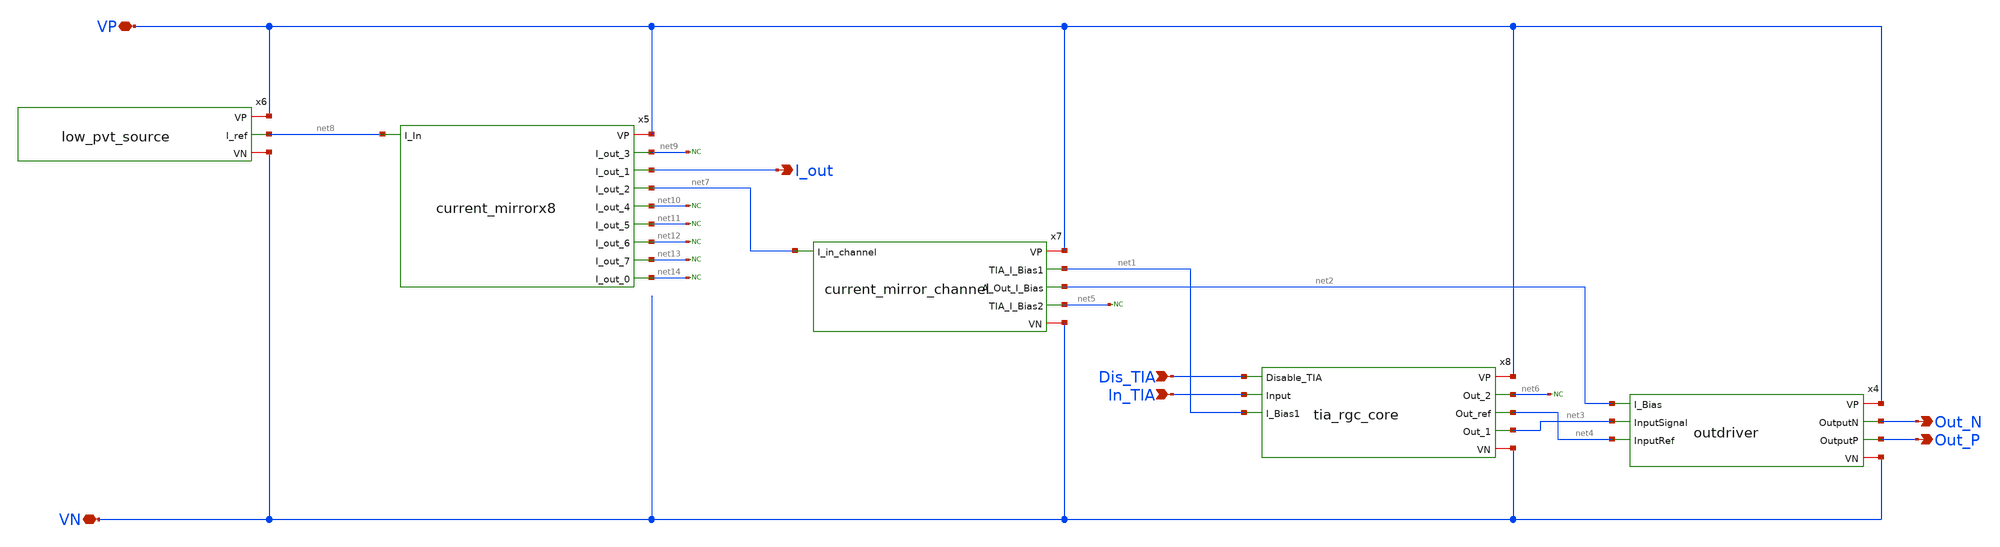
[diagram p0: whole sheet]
** sch_path: xschem/mpw5_submission.sch
**.subckt mpw5_submission VP In_TIA Out_N VN Out_P Dis_TIA I_out
*.iopin VP
*.ipin In_TIA
*.opin Out_N
*.iopin VN
*.opin Out_P
*.ipin Dis_TIA
*.opin I_out
x4 VP Out_N Out_P net2 net3 net4 VN outdriver
x5 VP net9 I_out net7 net8 net10 net11 net12 net13 net14 current_mirrorx8
x6 VP net8 VN low_pvt_source
x7 VP net1 net2 net5 net7 VN current_mirror_channel
x8 VP net6 net4 net3 Dis_TIA In_TIA net1 VN tia_rgc_core
* noconn #net5
* noconn #net6
* noconn #net9
* noconn #net10
* noconn #net11
* noconn #net12
* noconn #net13
* noconn #net14
**.ends

* expanding   symbol:  outdriver/outdriver.sym # of pins=7
** sym_path: xschem/outdriver/outdriver.sym
** sch_path: xschem/outdriver/outdriver.sch
.subckt outdriver VP OutputN OutputP I_Bias InputSignal InputRef VN
*.iopin VN
*.ipin InputRef
*.iopin VP
*.ipin I_Bias
*.ipin InputSignal
*.opin OutputN
*.opin OutputP
XM1 V_da1_P InputSignal VM6D VM6D sky130_fd_pr__nfet_01v8_lvt L=0.15 W=2 nf=1 ad='int((nf+1)/2) * W/nf * 0.29'
+ as='int((nf+2)/2) * W/nf * 0.29' pd='2*int((nf+1)/2) * (W/nf + 0.29)' ps='2*int((nf+2)/2) * (W/nf + 0.29)'
+ nrd='0.29 / W' nrs='0.29 / W' sa=0 sb=0 sd=0 mult=11*2 m=11*2
XM3 VM3D I_Bias VN VN sky130_fd_pr__nfet_01v8 L=0.5 W=2 nf=1 ad='int((nf+1)/2) * W/nf * 0.29' as='int((nf+2)/2) * W/nf * 0.29'
+ pd='2*int((nf+1)/2) * (W/nf + 0.29)' ps='2*int((nf+2)/2) * (W/nf + 0.29)' nrd='0.29 / W' nrs='0.29 / W'
+ sa=0 sb=0 sd=0 mult=2*(64) m=2*(64)
XM6 VM6D I_Bias VM3D VN sky130_fd_pr__nfet_01v8 L=0.15 W=2 nf=1 ad='int((nf+1)/2) * W/nf * 0.29' as='int((nf+2)/2) * W/nf * 0.29'
+ pd='2*int((nf+1)/2) * (W/nf + 0.29)' ps='2*int((nf+2)/2) * (W/nf + 0.29)' nrd='0.29 / W' nrs='0.29 / W'
+ sa=0 sb=0 sd=0 mult=64 m=64
XM7 I_Bias I_Bias net1 VN sky130_fd_pr__nfet_01v8 L=0.15 W=2 nf=1 ad='int((nf+1)/2) * W/nf * 0.29' as='int((nf+2)/2) * W/nf * 0.29'
+ pd='2*int((nf+1)/2) * (W/nf + 0.29)' ps='2*int((nf+2)/2) * (W/nf + 0.29)' nrd='0.29 / W' nrs='0.29 / W'
+ sa=0 sb=0 sd=0 mult=2 m=2
XM8 net1 I_Bias VN VN sky130_fd_pr__nfet_01v8 L=0.5 W=2 nf=1 ad='int((nf+1)/2) * W/nf * 0.29' as='int((nf+2)/2) * W/nf * 0.29'
+ pd='2*int((nf+1)/2) * (W/nf + 0.29)' ps='2*int((nf+2)/2) * (W/nf + 0.29)' nrd='0.29 / W' nrs='0.29 / W'
+ sa=0 sb=0 sd=0 mult=2*2 m=2*2
XM2 V_da2_P V_da1_P VM1_D VM1_D sky130_fd_pr__nfet_01v8_lvt L=0.15 W=2 nf=1 ad='int((nf+1)/2) * W/nf * 0.29'
+ as='int((nf+2)/2) * W/nf * 0.29' pd='2*int((nf+1)/2) * (W/nf + 0.29)' ps='2*int((nf+2)/2) * (W/nf + 0.29)'
+ nrd='0.29 / W' nrs='0.29 / W' sa=0 sb=0 sd=0 mult=44*2 m=44*2
XM4 V_da2_N V_da1_N VM1_D VM1_D sky130_fd_pr__nfet_01v8_lvt L=0.15 W=2 nf=1 ad='int((nf+1)/2) * W/nf * 0.29'
+ as='int((nf+2)/2) * W/nf * 0.29' pd='2*int((nf+1)/2) * (W/nf + 0.29)' ps='2*int((nf+2)/2) * (W/nf + 0.29)'
+ nrd='0.29 / W' nrs='0.29 / W' sa=0 sb=0 sd=0 mult=44*2 m=44*2
XM9 net2 I_Bias VN VN sky130_fd_pr__nfet_01v8 L=0.5 W=2 nf=1 ad='int((nf+1)/2) * W/nf * 0.29' as='int((nf+2)/2) * W/nf * 0.29'
+ pd='2*int((nf+1)/2) * (W/nf + 0.29)' ps='2*int((nf+2)/2) * (W/nf + 0.29)' nrd='0.29 / W' nrs='0.29 / W'
+ sa=0 sb=0 sd=0 mult=2*(256+64) m=2*(256+64)
XM10 VM1_D I_Bias net2 VN sky130_fd_pr__nfet_01v8 L=0.15 W=2 nf=1 ad='int((nf+1)/2) * W/nf * 0.29' as='int((nf+2)/2) * W/nf * 0.29'
+ pd='2*int((nf+1)/2) * (W/nf + 0.29)' ps='2*int((nf+2)/2) * (W/nf + 0.29)' nrd='0.29 / W' nrs='0.29 / W'
+ sa=0 sb=0 sd=0 mult=256+64 m=256+64
XM11 OutputP V_da2_P VM14D VM14D sky130_fd_pr__nfet_01v8_lvt L=0.15 W=2 nf=1 ad='int((nf+1)/2) * W/nf * 0.29'
+ as='int((nf+2)/2) * W/nf * 0.29' pd='2*int((nf+1)/2) * (W/nf + 0.29)' ps='2*int((nf+2)/2) * (W/nf + 0.29)'
+ nrd='0.29 / W' nrs='0.29 / W' sa=0 sb=0 sd=0 mult=44*4*2 m=44*4*2
XM12 OutputN V_da2_N VM14D VM14D sky130_fd_pr__nfet_01v8_lvt L=0.15 W=2 nf=1 ad='int((nf+1)/2) * W/nf * 0.29'
+ as='int((nf+2)/2) * W/nf * 0.29' pd='2*int((nf+1)/2) * (W/nf + 0.29)' ps='2*int((nf+2)/2) * (W/nf + 0.29)'
+ nrd='0.29 / W' nrs='0.29 / W' sa=0 sb=0 sd=0 mult=44*4*2 m=44*4*2
XM13 net3 I_Bias VN VN sky130_fd_pr__nfet_01v8 L=0.5 W=2 nf=1 ad='int((nf+1)/2) * W/nf * 0.29' as='int((nf+2)/2) * W/nf * 0.29'
+ pd='2*int((nf+1)/2) * (W/nf + 0.29)' ps='2*int((nf+2)/2) * (W/nf + 0.29)' nrd='0.29 / W' nrs='0.29 / W'
+ sa=0 sb=0 sd=0 mult=2*(1024+256) m=2*(1024+256)
XM14 VM14D I_Bias net3 VN sky130_fd_pr__nfet_01v8 L=0.15 W=2 nf=1 ad='int((nf+1)/2) * W/nf * 0.29' as='int((nf+2)/2) * W/nf * 0.29'
+ pd='2*int((nf+1)/2) * (W/nf + 0.29)' ps='2*int((nf+2)/2) * (W/nf + 0.29)' nrd='0.29 / W' nrs='0.29 / W'
+ sa=0 sb=0 sd=0 mult=1024+256 m=1024+256
XR7 V_da2_N VP VN sky130_fd_pr__res_high_po_5p73 L=4 mult=4*2 m=4*2
XR5 V_da2_P VP VN sky130_fd_pr__res_high_po_5p73 L=4 mult=4*2 m=4*2
XR3 V_da1_N VP VN sky130_fd_pr__res_high_po_2p85 L=6 mult=4 m=4
XR4 V_da1_P VP VN sky130_fd_pr__res_high_po_2p85 L=6 mult=4 m=4
XC2 InputRef VN sky130_fd_pr__cap_mim_m3_2 W=30 L=30 MF=1 m=1
XM5 V_da1_N InputRef VM6D VM6D sky130_fd_pr__nfet_01v8_lvt L=0.15 W=2 nf=1 ad='int((nf+1)/2) * W/nf * 0.29'
+ as='int((nf+2)/2) * W/nf * 0.29' pd='2*int((nf+1)/2) * (W/nf + 0.29)' ps='2*int((nf+2)/2) * (W/nf + 0.29)'
+ nrd='0.29 / W' nrs='0.29 / W' sa=0 sb=0 sd=0 mult=11*2 m=11*2
XR8 OutputP VP VN sky130_fd_pr__res_high_po_5p73 L=4 mult=16*2 m=16*2
XC1 InputRef VN sky130_fd_pr__cap_mim_m3_2 W=30 L=30 MF=1 m=1
XC6 VN VP sky130_fd_pr__cap_mim_m3_2 W=30 L=30 MF=1 m=1
XC8 VN VP sky130_fd_pr__cap_mim_m3_2 W=30 L=30 MF=1 m=1
XR1 OutputN VP VN sky130_fd_pr__res_high_po_5p73 L=4 mult=16*2 m=16*2
XC7 VN VP sky130_fd_pr__cap_mim_m3_2 W=30 L=30 MF=1 m=1
XC9 VN VP sky130_fd_pr__cap_mim_m3_2 W=30 L=30 MF=1 m=1
XC10 VN VP sky130_fd_pr__cap_mim_m3_2 W=30 L=30 MF=1 m=1
XC11 VN VP sky130_fd_pr__cap_mim_m3_2 W=30 L=30 MF=1 m=1
XC12 VN VP sky130_fd_pr__cap_mim_m3_2 W=30 L=30 MF=1 m=1
XC13 VN VP sky130_fd_pr__cap_mim_m3_2 W=30 L=30 MF=1 m=1
XC14 VN VP sky130_fd_pr__cap_mim_m3_2 W=30 L=30 MF=1 m=1
XC5 VN I_Bias sky130_fd_pr__cap_mim_m3_1 W=20 L=20 MF=1 m=1
XC3 VN I_Bias sky130_fd_pr__cap_mim_m3_1 W=20 L=20 MF=1 m=1
.ends


* expanding   symbol:  bias/current_mirrorx8.sym # of pins=10
** sym_path: xschem/bias/current_mirrorx8.sym
** sch_path: xschem/bias/current_mirrorx8.sch
.subckt current_mirrorx8 VP I_out_3 I_out_1 I_out_2 I_In I_out_4 I_out_5 I_out_6 I_out_7 I_out_0
*.opin I_out_0
*.ipin I_In
*.iopin VP
*.opin I_out_1
*.opin I_out_2
*.opin I_out_3
*.opin I_out_4
*.opin I_out_5
*.opin I_out_6
*.opin I_out_7
XM1 net1 I_In VP VP sky130_fd_pr__pfet_01v8 L=1 W=2 nf=1 ad='int((nf+1)/2) * W/nf * 0.29' as='int((nf+2)/2) * W/nf * 0.29'
+ pd='2*int((nf+1)/2) * (W/nf + 0.29)' ps='2*int((nf+2)/2) * (W/nf + 0.29)' nrd='0.29 / W' nrs='0.29 / W'
+ sa=0 sb=0 sd=0 mult=4*4 m=4*4
XM2 I_In I_In net1 VP sky130_fd_pr__pfet_01v8 L=0.2 W=2 nf=1 ad='int((nf+1)/2) * W/nf * 0.29' as='int((nf+2)/2) * W/nf * 0.29'
+ pd='2*int((nf+1)/2) * (W/nf + 0.29)' ps='2*int((nf+2)/2) * (W/nf + 0.29)' nrd='0.29 / W' nrs='0.29 / W'
+ sa=0 sb=0 sd=0 mult=4 m=4
XM3 net2 I_In VP VP sky130_fd_pr__pfet_01v8 L=1 W=2 nf=1 ad='int((nf+1)/2) * W/nf * 0.29' as='int((nf+2)/2) * W/nf * 0.29'
+ pd='2*int((nf+1)/2) * (W/nf + 0.29)' ps='2*int((nf+2)/2) * (W/nf + 0.29)' nrd='0.29 / W' nrs='0.29 / W'
+ sa=0 sb=0 sd=0 mult=4*4 m=4*4
XM4 I_out_0 I_In net2 VP sky130_fd_pr__pfet_01v8 L=0.2 W=2 nf=1 ad='int((nf+1)/2) * W/nf * 0.29' as='int((nf+2)/2) * W/nf * 0.29'
+ pd='2*int((nf+1)/2) * (W/nf + 0.29)' ps='2*int((nf+2)/2) * (W/nf + 0.29)' nrd='0.29 / W' nrs='0.29 / W'
+ sa=0 sb=0 sd=0 mult=4 m=4
XM5 net3 I_In VP VP sky130_fd_pr__pfet_01v8 L=1 W=2 nf=1 ad='int((nf+1)/2) * W/nf * 0.29' as='int((nf+2)/2) * W/nf * 0.29'
+ pd='2*int((nf+1)/2) * (W/nf + 0.29)' ps='2*int((nf+2)/2) * (W/nf + 0.29)' nrd='0.29 / W' nrs='0.29 / W'
+ sa=0 sb=0 sd=0 mult=4*4 m=4*4
XM6 I_out_1 I_In net3 VP sky130_fd_pr__pfet_01v8 L=0.2 W=2 nf=1 ad='int((nf+1)/2) * W/nf * 0.29' as='int((nf+2)/2) * W/nf * 0.29'
+ pd='2*int((nf+1)/2) * (W/nf + 0.29)' ps='2*int((nf+2)/2) * (W/nf + 0.29)' nrd='0.29 / W' nrs='0.29 / W'
+ sa=0 sb=0 sd=0 mult=4 m=4
XM7 net4 I_In VP VP sky130_fd_pr__pfet_01v8 L=1 W=2 nf=1 ad='int((nf+1)/2) * W/nf * 0.29' as='int((nf+2)/2) * W/nf * 0.29'
+ pd='2*int((nf+1)/2) * (W/nf + 0.29)' ps='2*int((nf+2)/2) * (W/nf + 0.29)' nrd='0.29 / W' nrs='0.29 / W'
+ sa=0 sb=0 sd=0 mult=4*4 m=4*4
XM8 I_out_2 I_In net4 VP sky130_fd_pr__pfet_01v8 L=0.2 W=2 nf=1 ad='int((nf+1)/2) * W/nf * 0.29' as='int((nf+2)/2) * W/nf * 0.29'
+ pd='2*int((nf+1)/2) * (W/nf + 0.29)' ps='2*int((nf+2)/2) * (W/nf + 0.29)' nrd='0.29 / W' nrs='0.29 / W'
+ sa=0 sb=0 sd=0 mult=4 m=4
XM9 net5 I_In VP VP sky130_fd_pr__pfet_01v8 L=1 W=2 nf=1 ad='int((nf+1)/2) * W/nf * 0.29' as='int((nf+2)/2) * W/nf * 0.29'
+ pd='2*int((nf+1)/2) * (W/nf + 0.29)' ps='2*int((nf+2)/2) * (W/nf + 0.29)' nrd='0.29 / W' nrs='0.29 / W'
+ sa=0 sb=0 sd=0 mult=4*4 m=4*4
XM10 I_out_3 I_In net5 VP sky130_fd_pr__pfet_01v8 L=0.2 W=2 nf=1 ad='int((nf+1)/2) * W/nf * 0.29' as='int((nf+2)/2) * W/nf * 0.29'
+ pd='2*int((nf+1)/2) * (W/nf + 0.29)' ps='2*int((nf+2)/2) * (W/nf + 0.29)' nrd='0.29 / W' nrs='0.29 / W'
+ sa=0 sb=0 sd=0 mult=4 m=4
XM11 net6 I_In VP VP sky130_fd_pr__pfet_01v8 L=1 W=2 nf=1 ad='int((nf+1)/2) * W/nf * 0.29' as='int((nf+2)/2) * W/nf * 0.29'
+ pd='2*int((nf+1)/2) * (W/nf + 0.29)' ps='2*int((nf+2)/2) * (W/nf + 0.29)' nrd='0.29 / W' nrs='0.29 / W'
+ sa=0 sb=0 sd=0 mult=4*4 m=4*4
XM12 I_out_4 I_In net6 VP sky130_fd_pr__pfet_01v8 L=0.2 W=2 nf=1 ad='int((nf+1)/2) * W/nf * 0.29' as='int((nf+2)/2) * W/nf * 0.29'
+ pd='2*int((nf+1)/2) * (W/nf + 0.29)' ps='2*int((nf+2)/2) * (W/nf + 0.29)' nrd='0.29 / W' nrs='0.29 / W'
+ sa=0 sb=0 sd=0 mult=4 m=4
XM13 net7 I_In VP VP sky130_fd_pr__pfet_01v8 L=1 W=2 nf=1 ad='int((nf+1)/2) * W/nf * 0.29' as='int((nf+2)/2) * W/nf * 0.29'
+ pd='2*int((nf+1)/2) * (W/nf + 0.29)' ps='2*int((nf+2)/2) * (W/nf + 0.29)' nrd='0.29 / W' nrs='0.29 / W'
+ sa=0 sb=0 sd=0 mult=4*4 m=4*4
XM14 I_out_5 I_In net7 VP sky130_fd_pr__pfet_01v8 L=0.2 W=2 nf=1 ad='int((nf+1)/2) * W/nf * 0.29' as='int((nf+2)/2) * W/nf * 0.29'
+ pd='2*int((nf+1)/2) * (W/nf + 0.29)' ps='2*int((nf+2)/2) * (W/nf + 0.29)' nrd='0.29 / W' nrs='0.29 / W'
+ sa=0 sb=0 sd=0 mult=4 m=4
XM15 net8 I_In VP VP sky130_fd_pr__pfet_01v8 L=1 W=2 nf=1 ad='int((nf+1)/2) * W/nf * 0.29' as='int((nf+2)/2) * W/nf * 0.29'
+ pd='2*int((nf+1)/2) * (W/nf + 0.29)' ps='2*int((nf+2)/2) * (W/nf + 0.29)' nrd='0.29 / W' nrs='0.29 / W'
+ sa=0 sb=0 sd=0 mult=4*4 m=4*4
XM16 I_out_6 I_In net8 VP sky130_fd_pr__pfet_01v8 L=0.2 W=2 nf=1 ad='int((nf+1)/2) * W/nf * 0.29' as='int((nf+2)/2) * W/nf * 0.29'
+ pd='2*int((nf+1)/2) * (W/nf + 0.29)' ps='2*int((nf+2)/2) * (W/nf + 0.29)' nrd='0.29 / W' nrs='0.29 / W'
+ sa=0 sb=0 sd=0 mult=4 m=4
XM17 net9 I_In VP VP sky130_fd_pr__pfet_01v8 L=1 W=2 nf=1 ad='int((nf+1)/2) * W/nf * 0.29' as='int((nf+2)/2) * W/nf * 0.29'
+ pd='2*int((nf+1)/2) * (W/nf + 0.29)' ps='2*int((nf+2)/2) * (W/nf + 0.29)' nrd='0.29 / W' nrs='0.29 / W'
+ sa=0 sb=0 sd=0 mult=4*4 m=4*4
XM18 I_out_7 I_In net9 VP sky130_fd_pr__pfet_01v8 L=0.2 W=2 nf=1 ad='int((nf+1)/2) * W/nf * 0.29' as='int((nf+2)/2) * W/nf * 0.29'
+ pd='2*int((nf+1)/2) * (W/nf + 0.29)' ps='2*int((nf+2)/2) * (W/nf + 0.29)' nrd='0.29 / W' nrs='0.29 / W'
+ sa=0 sb=0 sd=0 mult=4 m=4
.ends


* expanding   symbol:  bias/low_pvt_source.sym # of pins=3
** sym_path: xschem/bias/low_pvt_source.sym
** sch_path: xschem/bias/low_pvt_source.sch
.subckt low_pvt_source VP I_ref VN
*.iopin VP
*.opin I_ref
*.iopin VN
XM1 VM1D VM8D VP VP sky130_fd_pr__pfet_01v8 L=1 W=4 nf=1 ad='int((nf+1)/2) * W/nf * 0.29' as='int((nf+2)/2) * W/nf * 0.29'
+ pd='2*int((nf+1)/2) * (W/nf + 0.29)' ps='2*int((nf+2)/2) * (W/nf + 0.29)' nrd='0.29 / W' nrs='0.29 / W'
+ sa=0 sb=0 sd=0 mult=10 m=10
XM2 VM2D VM2D VN VN sky130_fd_pr__nfet_01v8 L=6 W=4 nf=1 ad='int((nf+1)/2) * W/nf * 0.29' as='int((nf+2)/2) * W/nf * 0.29'
+ pd='2*int((nf+1)/2) * (W/nf + 0.29)' ps='2*int((nf+2)/2) * (W/nf + 0.29)' nrd='0.29 / W' nrs='0.29 / W'
+ sa=0 sb=0 sd=0 mult=30 m=30
XM5 VM9D VM8D VM1D VP sky130_fd_pr__pfet_01v8 L=0.2 W=4 nf=1 ad='int((nf+1)/2) * W/nf * 0.29' as='int((nf+2)/2) * W/nf * 0.29'
+ pd='2*int((nf+1)/2) * (W/nf + 0.29)' ps='2*int((nf+2)/2) * (W/nf + 0.29)' nrd='0.29 / W' nrs='0.29 / W'
+ sa=0 sb=0 sd=0 mult=2 m=2
XM11 VM11D VM2D VM12D VN sky130_fd_pr__nfet_01v8 L=6 W=4 nf=1 ad='int((nf+1)/2) * W/nf * 0.29' as='int((nf+2)/2) * W/nf * 0.29'
+ pd='2*int((nf+1)/2) * (W/nf + 0.29)' ps='2*int((nf+2)/2) * (W/nf + 0.29)' nrd='0.29 / W' nrs='0.29 / W'
+ sa=0 sb=0 sd=0 mult=65 m=65
XM12 VM12D VM12G VN VN sky130_fd_pr__nfet_01v8 L=6 W=4 nf=1 ad='int((nf+1)/2) * W/nf * 0.29' as='int((nf+2)/2) * W/nf * 0.29'
+ pd='2*int((nf+1)/2) * (W/nf + 0.29)' ps='2*int((nf+2)/2) * (W/nf + 0.29)' nrd='0.29 / W' nrs='0.29 / W'
+ sa=0 sb=0 sd=0 mult=2 m=2
XM14 VM14D VM12G VN VN sky130_fd_pr__nfet_01v8 L=6 W=4 nf=1 ad='int((nf+1)/2) * W/nf * 0.29' as='int((nf+2)/2) * W/nf * 0.29'
+ pd='2*int((nf+1)/2) * (W/nf + 0.29)' ps='2*int((nf+2)/2) * (W/nf + 0.29)' nrd='0.29 / W' nrs='0.29 / W'
+ sa=0 sb=0 sd=0 mult=2 m=2
XM16 VM16D VM8D VP VP sky130_fd_pr__pfet_01v8 L=1 W=4 nf=1 ad='int((nf+1)/2) * W/nf * 0.29' as='int((nf+2)/2) * W/nf * 0.29'
+ pd='2*int((nf+1)/2) * (W/nf + 0.29)' ps='2*int((nf+2)/2) * (W/nf + 0.29)' nrd='0.29 / W' nrs='0.29 / W'
+ sa=0 sb=0 sd=0 mult=10 m=10
XM17 VM8D VM8D VM16D VP sky130_fd_pr__pfet_01v8 L=0.2 W=4 nf=1 ad='int((nf+1)/2) * W/nf * 0.29' as='int((nf+2)/2) * W/nf * 0.29'
+ pd='2*int((nf+1)/2) * (W/nf + 0.29)' ps='2*int((nf+2)/2) * (W/nf + 0.29)' nrd='0.29 / W' nrs='0.29 / W'
+ sa=0 sb=0 sd=0 mult=2 m=2
XM18 VM18D VM8D VP VP sky130_fd_pr__pfet_01v8 L=1 W=4 nf=1 ad='int((nf+1)/2) * W/nf * 0.29' as='int((nf+2)/2) * W/nf * 0.29'
+ pd='2*int((nf+1)/2) * (W/nf + 0.29)' ps='2*int((nf+2)/2) * (W/nf + 0.29)' nrd='0.29 / W' nrs='0.29 / W'
+ sa=0 sb=0 sd=0 mult=10*3*2 m=10*3*2
XM19 VM14D VM8D VM18D VP sky130_fd_pr__pfet_01v8 L=0.2 W=4 nf=1 ad='int((nf+1)/2) * W/nf * 0.29' as='int((nf+2)/2) * W/nf * 0.29'
+ pd='2*int((nf+1)/2) * (W/nf + 0.29)' ps='2*int((nf+2)/2) * (W/nf + 0.29)' nrd='0.29 / W' nrs='0.29 / W'
+ sa=0 sb=0 sd=0 mult=2*3*2 m=2*3*2
XM20 VM20D VM8D VP VP sky130_fd_pr__pfet_01v8 L=1 W=4 nf=1 ad='int((nf+1)/2) * W/nf * 0.29' as='int((nf+2)/2) * W/nf * 0.29'
+ pd='2*int((nf+1)/2) * (W/nf + 0.29)' ps='2*int((nf+2)/2) * (W/nf + 0.29)' nrd='0.29 / W' nrs='0.29 / W'
+ sa=0 sb=0 sd=0 mult=10*1*1 m=10*1*1
XM21 VM22D VM8D VM20D VP sky130_fd_pr__pfet_01v8 L=0.2 W=4 nf=1 ad='int((nf+1)/2) * W/nf * 0.29' as='int((nf+2)/2) * W/nf * 0.29'
+ pd='2*int((nf+1)/2) * (W/nf + 0.29)' ps='2*int((nf+2)/2) * (W/nf + 0.29)' nrd='0.29 / W' nrs='0.29 / W'
+ sa=0 sb=0 sd=0 mult=2*1*1 m=2*1*1
XM22 VM22D VM4S VM3D VN sky130_fd_pr__nfet_01v8 L=6 W=4 nf=1 ad='int((nf+1)/2) * W/nf * 0.29' as='int((nf+2)/2) * W/nf * 0.29'
+ pd='2*int((nf+1)/2) * (W/nf + 0.29)' ps='2*int((nf+2)/2) * (W/nf + 0.29)' nrd='0.29 / W' nrs='0.29 / W'
+ sa=0 sb=0 sd=0 mult=20 m=20
XM3 VM3D VM3G VN VN sky130_fd_pr__nfet_01v8 L=6 W=4 nf=1 ad='int((nf+1)/2) * W/nf * 0.29' as='int((nf+2)/2) * W/nf * 0.29'
+ pd='2*int((nf+1)/2) * (W/nf + 0.29)' ps='2*int((nf+2)/2) * (W/nf + 0.29)' nrd='0.29 / W' nrs='0.29 / W'
+ sa=0 sb=0 sd=0 mult=4 m=4
XM13 VP VM14D VM12G VM12G sky130_fd_pr__nfet_01v8_lvt L=0.15 W=4 nf=1 ad='int((nf+1)/2) * W/nf * 0.29'
+ as='int((nf+2)/2) * W/nf * 0.29' pd='2*int((nf+1)/2) * (W/nf + 0.29)' ps='2*int((nf+2)/2) * (W/nf + 0.29)'
+ nrd='0.29 / W' nrs='0.29 / W' sa=0 sb=0 sd=0 mult=20 m=20
XM4 I_ref VM22D VM4S VN sky130_fd_pr__nfet_01v8_lvt L=0.15 W=4 nf=1 ad='int((nf+1)/2) * W/nf * 0.29'
+ as='int((nf+2)/2) * W/nf * 0.29' pd='2*int((nf+1)/2) * (W/nf + 0.29)' ps='2*int((nf+2)/2) * (W/nf + 0.29)'
+ nrd='0.29 / W' nrs='0.29 / W' sa=0 sb=0 sd=0 mult=20 m=20
XM48 VM50D VM11D VP VP sky130_fd_pr__pfet_01v8 L=2 W=0.5 nf=1 ad='int((nf+1)/2) * W/nf * 0.29' as='int((nf+2)/2) * W/nf * 0.29'
+ pd='2*int((nf+1)/2) * (W/nf + 0.29)' ps='2*int((nf+2)/2) * (W/nf + 0.29)' nrd='0.29 / W' nrs='0.29 / W'
+ sa=0 sb=0 sd=0 mult=1 m=1
XM50 VM50D VM11D VN VN sky130_fd_pr__nfet_01v8_lvt L=0.2 W=4 nf=1 ad='int((nf+1)/2) * W/nf * 0.29' as='int((nf+2)/2) * W/nf * 0.29'
+ pd='2*int((nf+1)/2) * (W/nf + 0.29)' ps='2*int((nf+2)/2) * (W/nf + 0.29)' nrd='0.29 / W' nrs='0.29 / W'
+ sa=0 sb=0 sd=0 mult=10 m=10
XC3 VP VM8D sky130_fd_pr__cap_mim_m3_1 W=20 L=20 MF=1 m=1
XM8 VM8D VM9D VM11D VM11D sky130_fd_pr__nfet_01v8_lvt L=1 W=4 nf=1 ad='int((nf+1)/2) * W/nf * 0.29' as='int((nf+2)/2) * W/nf * 0.29'
+ pd='2*int((nf+1)/2) * (W/nf + 0.29)' ps='2*int((nf+2)/2) * (W/nf + 0.29)' nrd='0.29 / W' nrs='0.29 / W'
+ sa=0 sb=0 sd=0 mult=20 m=20
XM9 VM9D VM9D VM2D VM2D sky130_fd_pr__nfet_01v8_lvt L=1 W=4 nf=1 ad='int((nf+1)/2) * W/nf * 0.29' as='int((nf+2)/2) * W/nf * 0.29'
+ pd='2*int((nf+1)/2) * (W/nf + 0.29)' ps='2*int((nf+2)/2) * (W/nf + 0.29)' nrd='0.29 / W' nrs='0.29 / W'
+ sa=0 sb=0 sd=0 mult=20 m=20
XM10 VM8D VM50D VN VN sky130_fd_pr__nfet_01v8 L=2 W=0.5 nf=1 ad='int((nf+1)/2) * W/nf * 0.29' as='int((nf+2)/2) * W/nf * 0.29'
+ pd='2*int((nf+1)/2) * (W/nf + 0.29)' ps='2*int((nf+2)/2) * (W/nf + 0.29)' nrd='0.29 / W' nrs='0.29 / W'
+ sa=0 sb=0 sd=0 mult=1 m=1
XC4 VN VP sky130_fd_pr__cap_mim_m3_2 W=30 L=30 MF=1 m=1
XR7 net3 VM4S VN sky130_fd_pr__res_xhigh_po_1p41 L=10 mult=1 m=1
XR3 net4 net3 VN sky130_fd_pr__res_xhigh_po_1p41 L=10 mult=1 m=1
XR4 net2 net4 VN sky130_fd_pr__res_xhigh_po_1p41 L=10 mult=1 m=1
XR5 net1 net2 VN sky130_fd_pr__res_xhigh_po_1p41 L=10 mult=1 m=1
XR6 VN net1 VN sky130_fd_pr__res_xhigh_po_1p41 L=10 mult=1 m=1
XR8 net5 VM12G VN sky130_fd_pr__res_xhigh_po_1p41 L=10 mult=1 m=1
XR1 net5 VM3G VN sky130_fd_pr__res_xhigh_po_1p41 L=10 mult=1 m=1
XR2 net7 net6 VN sky130_fd_pr__res_xhigh_po_1p41 L=10 mult=1 m=1
XR9 VN net6 VN sky130_fd_pr__res_xhigh_po_1p41 L=10 mult=1 m=1
XR10 net11 net7 VN sky130_fd_pr__res_xhigh_po_1p41 L=10 mult=1 m=1
XR11 net12 net11 VN sky130_fd_pr__res_xhigh_po_1p41 L=10 mult=1 m=1
XR12 net8 net12 VN sky130_fd_pr__res_xhigh_po_1p41 L=10 mult=1 m=1
XR13 net10 VM3G VN sky130_fd_pr__res_xhigh_po_1p41 L=10 mult=1 m=1
XR14 net9 net10 VN sky130_fd_pr__res_xhigh_po_1p41 L=10 mult=1 m=1
XR15 net8 net9 VN sky130_fd_pr__res_xhigh_po_1p41 L=10 mult=1 m=1
XC1 VN VP sky130_fd_pr__cap_mim_m3_2 W=30 L=30 MF=1 m=1
.ends


* expanding   symbol:  bias/current_mirror_channel.sym # of pins=6
** sym_path: xschem/bias/current_mirror_channel.sym
** sch_path: xschem/bias/current_mirror_channel.sch
.subckt current_mirror_channel VP TIA_I_Bias1 A_Out_I_Bias TIA_I_Bias2 I_in_channel VN
*.ipin I_in_channel
*.iopin VP
*.opin TIA_I_Bias2
*.iopin VN
*.opin TIA_I_Bias1
*.opin A_Out_I_Bias
XM1 I_in_channel I_in_channel net1 VN sky130_fd_pr__nfet_01v8 L=0.2 W=2 nf=1 ad='int((nf+1)/2) * W/nf * 0.29'
+ as='int((nf+2)/2) * W/nf * 0.29' pd='2*int((nf+1)/2) * (W/nf + 0.29)' ps='2*int((nf+2)/2) * (W/nf + 0.29)'
+ nrd='0.29 / W' nrs='0.29 / W' sa=0 sb=0 sd=0 mult=2 m=2
XM2 net5 net4 VP VP sky130_fd_pr__pfet_01v8 L=1 W=2 nf=1 ad='int((nf+1)/2) * W/nf * 0.29' as='int((nf+2)/2) * W/nf * 0.29'
+ pd='2*int((nf+1)/2) * (W/nf + 0.29)' ps='2*int((nf+2)/2) * (W/nf + 0.29)' nrd='0.29 / W' nrs='0.29 / W'
+ sa=0 sb=0 sd=0 mult=4*4 m=4*4
XM3 net1 I_in_channel VN VN sky130_fd_pr__nfet_01v8 L=1 W=2 nf=1 ad='int((nf+1)/2) * W/nf * 0.29' as='int((nf+2)/2) * W/nf * 0.29'
+ pd='2*int((nf+1)/2) * (W/nf + 0.29)' ps='2*int((nf+2)/2) * (W/nf + 0.29)' nrd='0.29 / W' nrs='0.29 / W'
+ sa=0 sb=0 sd=0 mult=2*4 m=2*4
XM4 net4 net4 net5 VP sky130_fd_pr__pfet_01v8 L=0.2 W=2 nf=1 ad='int((nf+1)/2) * W/nf * 0.29' as='int((nf+2)/2) * W/nf * 0.29'
+ pd='2*int((nf+1)/2) * (W/nf + 0.29)' ps='2*int((nf+2)/2) * (W/nf + 0.29)' nrd='0.29 / W' nrs='0.29 / W'
+ sa=0 sb=0 sd=0 mult=4 m=4
XC8 VP net4 sky130_fd_pr__cap_mim_m3_2 W=30 L=30 MF=1 m=1
XM5 net4 I_in_channel net2 VN sky130_fd_pr__nfet_01v8 L=0.2 W=2 nf=1 ad='int((nf+1)/2) * W/nf * 0.29'
+ as='int((nf+2)/2) * W/nf * 0.29' pd='2*int((nf+1)/2) * (W/nf + 0.29)' ps='2*int((nf+2)/2) * (W/nf + 0.29)'
+ nrd='0.29 / W' nrs='0.29 / W' sa=0 sb=0 sd=0 mult=2 m=2
XM6 TIA_I_Bias2 I_in_channel net3 VN sky130_fd_pr__nfet_01v8 L=0.2 W=2 nf=1 ad='int((nf+1)/2) * W/nf * 0.29'
+ as='int((nf+2)/2) * W/nf * 0.29' pd='2*int((nf+1)/2) * (W/nf + 0.29)' ps='2*int((nf+2)/2) * (W/nf + 0.29)'
+ nrd='0.29 / W' nrs='0.29 / W' sa=0 sb=0 sd=0 mult=2 m=2
XM7 net2 I_in_channel VN VN sky130_fd_pr__nfet_01v8 L=1 W=2 nf=1 ad='int((nf+1)/2) * W/nf * 0.29' as='int((nf+2)/2) * W/nf * 0.29'
+ pd='2*int((nf+1)/2) * (W/nf + 0.29)' ps='2*int((nf+2)/2) * (W/nf + 0.29)' nrd='0.29 / W' nrs='0.29 / W'
+ sa=0 sb=0 sd=0 mult=2*4 m=2*4
XM8 net3 I_in_channel VN VN sky130_fd_pr__nfet_01v8 L=1 W=2 nf=1 ad='int((nf+1)/2) * W/nf * 0.29' as='int((nf+2)/2) * W/nf * 0.29'
+ pd='2*int((nf+1)/2) * (W/nf + 0.29)' ps='2*int((nf+2)/2) * (W/nf + 0.29)' nrd='0.29 / W' nrs='0.29 / W'
+ sa=0 sb=0 sd=0 mult=2*4 m=2*4
XM13 net6 net4 VP VP sky130_fd_pr__pfet_01v8 L=1 W=2 nf=1 ad='int((nf+1)/2) * W/nf * 0.29' as='int((nf+2)/2) * W/nf * 0.29'
+ pd='2*int((nf+1)/2) * (W/nf + 0.29)' ps='2*int((nf+2)/2) * (W/nf + 0.29)' nrd='0.29 / W' nrs='0.29 / W'
+ sa=0 sb=0 sd=0 mult=4*4*10 m=4*4*10
XM14 TIA_I_Bias1 net4 net6 VP sky130_fd_pr__pfet_01v8 L=0.2 W=2 nf=1 ad='int((nf+1)/2) * W/nf * 0.29'
+ as='int((nf+2)/2) * W/nf * 0.29' pd='2*int((nf+1)/2) * (W/nf + 0.29)' ps='2*int((nf+2)/2) * (W/nf + 0.29)'
+ nrd='0.29 / W' nrs='0.29 / W' sa=0 sb=0 sd=0 mult=4*10 m=4*10
XM9 net7 net4 VP VP sky130_fd_pr__pfet_01v8 L=1 W=2 nf=1 ad='int((nf+1)/2) * W/nf * 0.29' as='int((nf+2)/2) * W/nf * 0.29'
+ pd='2*int((nf+1)/2) * (W/nf + 0.29)' ps='2*int((nf+2)/2) * (W/nf + 0.29)' nrd='0.29 / W' nrs='0.29 / W'
+ sa=0 sb=0 sd=0 mult=4*4*12 m=4*4*12
XM10 A_Out_I_Bias net4 net7 VP sky130_fd_pr__pfet_01v8 L=0.2 W=2 nf=1 ad='int((nf+1)/2) * W/nf * 0.29'
+ as='int((nf+2)/2) * W/nf * 0.29' pd='2*int((nf+1)/2) * (W/nf + 0.29)' ps='2*int((nf+2)/2) * (W/nf + 0.29)'
+ nrd='0.29 / W' nrs='0.29 / W' sa=0 sb=0 sd=0 mult=4*12 m=4*12
XC4 VP net4 sky130_fd_pr__cap_mim_m3_2 W=30 L=30 MF=1 m=1
XC3 VN I_in_channel sky130_fd_pr__cap_mim_m3_2 W=30 L=30 MF=1 m=1
XC6 VN I_in_channel sky130_fd_pr__cap_mim_m3_2 W=30 L=30 MF=1 m=1
XC1 VN VP sky130_fd_pr__cap_mim_m3_2 W=30 L=30 MF=1 m=1
XC2 VN VP sky130_fd_pr__cap_mim_m3_2 W=30 L=30 MF=1 m=1
.ends


* expanding   symbol:  tia/tia_rgc_core.sym # of pins=8
** sym_path: xschem/tia/tia_rgc_core.sym
** sch_path: xschem/tia/tia_rgc_core.sch
.subckt tia_rgc_core VP Out_2 Out_ref Out_1 Disable_TIA Input I_Bias1 VN
*.iopin VN
*.iopin VP
*.opin Out_2
*.ipin I_Bias1
*.ipin Input
*.ipin Disable_TIA
*.opin Out_1
*.opin Out_ref
XM5 VM5D I_Bias1 VN VN sky130_fd_pr__nfet_01v8 L=1 W=2 nf=1 ad='int((nf+1)/2) * W/nf * 0.29' as='int((nf+2)/2) * W/nf * 0.29'
+ pd='2*int((nf+1)/2) * (W/nf + 0.29)' ps='2*int((nf+2)/2) * (W/nf + 0.29)' nrd='0.29 / W' nrs='0.29 / W'
+ sa=0 sb=0 sd=0 mult=6 m=6
XM6 VM6D I_Bias1 VN VN sky130_fd_pr__nfet_01v8 L=1.0 W=2 nf=1 ad='int((nf+1)/2) * W/nf * 0.29' as='int((nf+2)/2) * W/nf * 0.29'
+ pd='2*int((nf+1)/2) * (W/nf + 0.29)' ps='2*int((nf+2)/2) * (W/nf + 0.29)' nrd='0.29 / W' nrs='0.29 / W'
+ sa=0 sb=0 sd=0 mult=6 m=6
XM7 Out_1 Input VM28D VN sky130_fd_pr__nfet_01v8_lvt L=0.2 W=2 nf=1 ad='int((nf+1)/2) * W/nf * 0.29'
+ as='int((nf+2)/2) * W/nf * 0.29' pd='2*int((nf+1)/2) * (W/nf + 0.29)' ps='2*int((nf+2)/2) * (W/nf + 0.29)'
+ nrd='0.29 / W' nrs='0.29 / W' sa=0 sb=0 sd=0 mult=100 m=100
XM8 Out_1 Input VP VP sky130_fd_pr__pfet_01v8 L=0.2 W=2 nf=1 ad='int((nf+1)/2) * W/nf * 0.29' as='int((nf+2)/2) * W/nf * 0.29'
+ pd='2*int((nf+1)/2) * (W/nf + 0.29)' ps='2*int((nf+2)/2) * (W/nf + 0.29)' nrd='0.29 / W' nrs='0.29 / W'
+ sa=0 sb=0 sd=0 mult=60 m=60
XM9 Input I_Bias1 VM5D VN sky130_fd_pr__nfet_01v8 L=0.15 W=2 nf=1 ad='int((nf+1)/2) * W/nf * 0.29' as='int((nf+2)/2) * W/nf * 0.29'
+ pd='2*int((nf+1)/2) * (W/nf + 0.29)' ps='2*int((nf+2)/2) * (W/nf + 0.29)' nrd='0.29 / W' nrs='0.29 / W'
+ sa=0 sb=0 sd=0 mult=12 m=12
XM10 I_Bias1 I_Bias1 VM6D VN sky130_fd_pr__nfet_01v8 L=0.15 W=2 nf=1 ad='int((nf+1)/2) * W/nf * 0.29'
+ as='int((nf+2)/2) * W/nf * 0.29' pd='2*int((nf+1)/2) * (W/nf + 0.29)' ps='2*int((nf+2)/2) * (W/nf + 0.29)'
+ nrd='0.29 / W' nrs='0.29 / W' sa=0 sb=0 sd=0 mult=12 m=12
XM23 I_Bias1 Disable_TIA VN VN sky130_fd_pr__nfet_01v8 L=0.15 W=2 nf=1 ad='int((nf+1)/2) * W/nf * 0.29'
+ as='int((nf+2)/2) * W/nf * 0.29' pd='2*int((nf+1)/2) * (W/nf + 0.29)' ps='2*int((nf+2)/2) * (W/nf + 0.29)'
+ nrd='0.29 / W' nrs='0.29 / W' sa=0 sb=0 sd=0 mult=5 m=5
XM26 Disable_TIA_B Disable_TIA VN VN sky130_fd_pr__nfet_01v8 L=1 W=0.5 nf=1 ad='int((nf+1)/2) * W/nf * 0.29'
+ as='int((nf+2)/2) * W/nf * 0.29' pd='2*int((nf+1)/2) * (W/nf + 0.29)' ps='2*int((nf+2)/2) * (W/nf + 0.29)'
+ nrd='0.29 / W' nrs='0.29 / W' sa=0 sb=0 sd=0 mult=1 m=1
XM27 Disable_TIA_B Disable_TIA VP VP sky130_fd_pr__pfet_01v8 L=1 W=0.5 nf=1 ad='int((nf+1)/2) * W/nf * 0.29'
+ as='int((nf+2)/2) * W/nf * 0.29' pd='2*int((nf+1)/2) * (W/nf + 0.29)' ps='2*int((nf+2)/2) * (W/nf + 0.29)'
+ nrd='0.29 / W' nrs='0.29 / W' sa=0 sb=0 sd=0 mult=1 m=1
XM28 VM28D Disable_TIA_B VN VN sky130_fd_pr__nfet_01v8 L=0.15 W=2 nf=1 ad='int((nf+1)/2) * W/nf * 0.29'
+ as='int((nf+2)/2) * W/nf * 0.29' pd='2*int((nf+1)/2) * (W/nf + 0.29)' ps='2*int((nf+2)/2) * (W/nf + 0.29)'
+ nrd='0.29 / W' nrs='0.29 / W' sa=0 sb=0 sd=0 mult=100 m=100
XM36 VM36D I_Bias1 VN VN sky130_fd_pr__nfet_01v8 L=1 W=2 nf=1 ad='int((nf+1)/2) * W/nf * 0.29' as='int((nf+2)/2) * W/nf * 0.29'
+ pd='2*int((nf+1)/2) * (W/nf + 0.29)' ps='2*int((nf+2)/2) * (W/nf + 0.29)' nrd='0.29 / W' nrs='0.29 / W'
+ sa=0 sb=0 sd=0 mult=6 m=6
XM37 Out_ref VM39D VM40D VN sky130_fd_pr__nfet_01v8_lvt L=0.2 W=2 nf=1 ad='int((nf+1)/2) * W/nf * 0.29'
+ as='int((nf+2)/2) * W/nf * 0.29' pd='2*int((nf+1)/2) * (W/nf + 0.29)' ps='2*int((nf+2)/2) * (W/nf + 0.29)'
+ nrd='0.29 / W' nrs='0.29 / W' sa=0 sb=0 sd=0 mult=100 m=100
XM38 Out_ref VM39D VP VP sky130_fd_pr__pfet_01v8 L=0.2 W=2 nf=1 ad='int((nf+1)/2) * W/nf * 0.29' as='int((nf+2)/2) * W/nf * 0.29'
+ pd='2*int((nf+1)/2) * (W/nf + 0.29)' ps='2*int((nf+2)/2) * (W/nf + 0.29)' nrd='0.29 / W' nrs='0.29 / W'
+ sa=0 sb=0 sd=0 mult=60 m=60
XM39 VM39D I_Bias1 VM36D VN sky130_fd_pr__nfet_01v8 L=0.15 W=2 nf=1 ad='int((nf+1)/2) * W/nf * 0.29'
+ as='int((nf+2)/2) * W/nf * 0.29' pd='2*int((nf+1)/2) * (W/nf + 0.29)' ps='2*int((nf+2)/2) * (W/nf + 0.29)'
+ nrd='0.29 / W' nrs='0.29 / W' sa=0 sb=0 sd=0 mult=12 m=12
XM40 VM40D Disable_TIA_B VN VN sky130_fd_pr__nfet_01v8 L=0.15 W=2 nf=1 ad='int((nf+1)/2) * W/nf * 0.29'
+ as='int((nf+2)/2) * W/nf * 0.29' pd='2*int((nf+1)/2) * (W/nf + 0.29)' ps='2*int((nf+2)/2) * (W/nf + 0.29)'
+ nrd='0.29 / W' nrs='0.29 / W' sa=0 sb=0 sd=0 mult=100 m=100
XC20 VP VN sky130_fd_pr__cap_mim_m3_2 W=30 L=30 MF=1 m=1
XM16 Out_2 VN VP VP sky130_fd_pr__pfet_01v8 L=0.5 W=2 nf=1 ad='int((nf+1)/2) * W/nf * 0.29' as='int((nf+2)/2) * W/nf * 0.29'
+ pd='2*int((nf+1)/2) * (W/nf + 0.29)' ps='2*int((nf+2)/2) * (W/nf + 0.29)' nrd='0.29 / W' nrs='0.29 / W'
+ sa=0 sb=0 sd=0 mult=10 m=10
XM15 Out_2 Out_1 Input Input sky130_fd_pr__nfet_01v8_lvt L=0.2 W=2 nf=1 ad='int((nf+1)/2) * W/nf * 0.29'
+ as='int((nf+2)/2) * W/nf * 0.29' pd='2*int((nf+1)/2) * (W/nf + 0.29)' ps='2*int((nf+2)/2) * (W/nf + 0.29)'
+ nrd='0.29 / W' nrs='0.29 / W' sa=0 sb=0 sd=0 mult=30 m=30
XM31 VM31D Out_ref VM39D VM39D sky130_fd_pr__nfet_01v8_lvt L=0.2 W=2 nf=1 ad='int((nf+1)/2) * W/nf * 0.29'
+ as='int((nf+2)/2) * W/nf * 0.29' pd='2*int((nf+1)/2) * (W/nf + 0.29)' ps='2*int((nf+2)/2) * (W/nf + 0.29)'
+ nrd='0.29 / W' nrs='0.29 / W' sa=0 sb=0 sd=0 mult=30 m=30
XM35 VM31D VN VP VP sky130_fd_pr__pfet_01v8 L=0.5 W=2 nf=1 ad='int((nf+1)/2) * W/nf * 0.29' as='int((nf+2)/2) * W/nf * 0.29'
+ pd='2*int((nf+1)/2) * (W/nf + 0.29)' ps='2*int((nf+2)/2) * (W/nf + 0.29)' nrd='0.29 / W' nrs='0.29 / W'
+ sa=0 sb=0 sd=0 mult=10 m=10
XC7 VP VN sky130_fd_pr__cap_mim_m3_2 W=30 L=30 MF=1 m=1
XC2 VP VM28D sky130_fd_pr__cap_mim_m3_2 W=25 L=18 MF=1 m=1
XC5 VN I_Bias1 sky130_fd_pr__cap_mim_m3_1 W=15 L=12 MF=1 m=1
XC4 VN I_Bias1 sky130_fd_pr__cap_mim_m3_1 W=15 L=12 MF=1 m=1
XC1 VP VM40D sky130_fd_pr__cap_mim_m3_2 W=25 L=18 MF=1 m=1
XC10 Disable_TIA_B VN VN sky130_fd_pr__cap_var_lvt W=5 L=2 VM=1 m=1
XC3 Disable_TIA_B VN VN sky130_fd_pr__cap_var_lvt W=5 L=2 VM=1 m=1
XC6 Disable_TIA_B VN VN sky130_fd_pr__cap_var_lvt W=5 L=2 VM=1 m=1
XC8 Disable_TIA_B VN VN sky130_fd_pr__cap_var_lvt W=5 L=2 VM=1 m=1
XC9 Disable_TIA_B VN VN sky130_fd_pr__cap_var_lvt W=5 L=2 VM=1 m=1
.ends

.end
